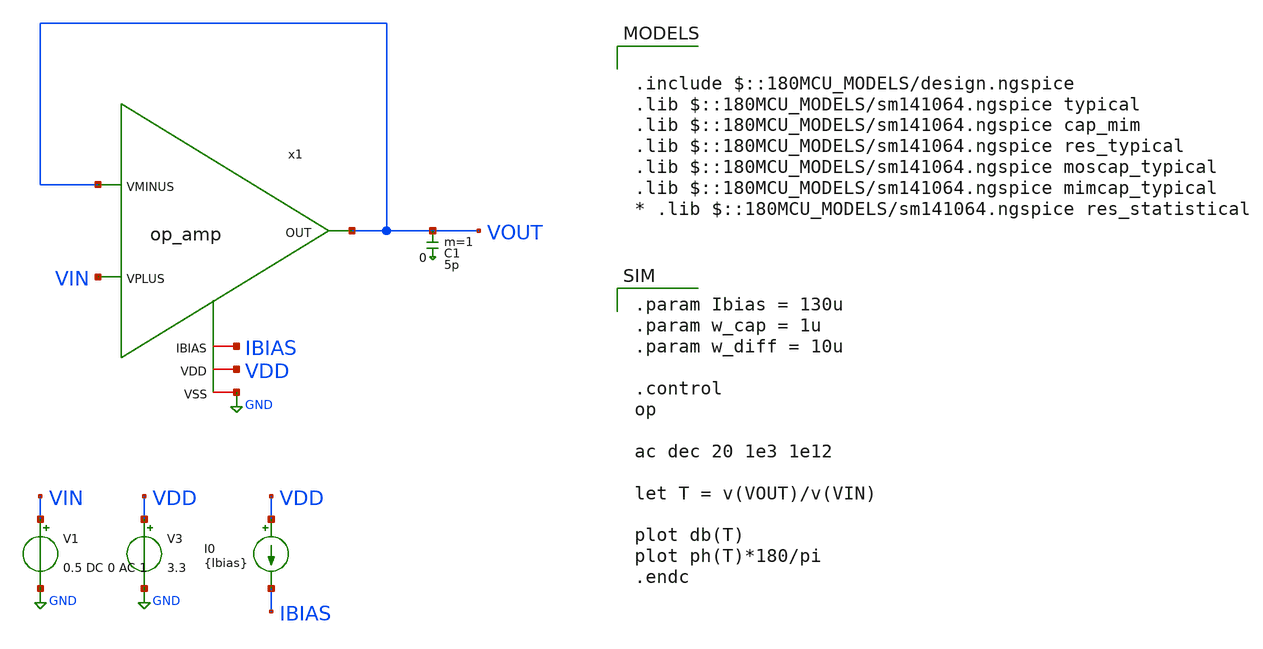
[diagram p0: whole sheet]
** sch_path: xschem/tb_op_amp.sch
**.subckt tb_op_amp
x1 VOUT VIN VOUT VDD GND IBIAS op_amp
V3 VDD GND 3.3
I0 VDD IBIAS {Ibias}
V1 VIN GND 0.5 DC 0 AC 1
C1 VOUT 0 5p m=1
**** begin user architecture code

.param Ibias = 130u
.param w_cap = 1u
.param w_diff = 10u

.control
op

ac dec 20 1e3 1e12

let T = v(VOUT)/v(VIN)

plot db(T)
plot ph(T)*180/pi
.endc



.include $::180MCU_MODELS/design.ngspice
.lib $::180MCU_MODELS/sm141064.ngspice typical
.lib $::180MCU_MODELS/sm141064.ngspice cap_mim
.lib $::180MCU_MODELS/sm141064.ngspice res_typical
.lib $::180MCU_MODELS/sm141064.ngspice moscap_typical
.lib $::180MCU_MODELS/sm141064.ngspice mimcap_typical
* .lib $::180MCU_MODELS/sm141064.ngspice res_statistical

**** end user architecture code
**.ends

* expanding   symbol:  op_amp.sym # of pins=6
** sym_path: xschem/op_amp.sym
** sch_path: xschem/op_amp.sch
.subckt op_amp OUT VPLUS VMINUS VDD VSS IBIAS
*.iopin VDD
*.iopin VSS
*.ipin VPLUS
*.ipin VMINUS
*.opin OUT
*.iopin IBIAS
XM1 net2 VMINUS net1 VSS nfet_03v3 L=0.5u W=4u nf=1 ad='int((nf+1)/2) * W/nf * 0.18u' as='int((nf+2)/2) * W/nf * 0.18u'
+ pd='2*int((nf+1)/2) * (W/nf + 0.18u)' ps='2*int((nf+2)/2) * (W/nf + 0.18u)' nrd='0.18u / W' nrs='0.18u / W'
+ sa=0 sb=0 sd=0 m=1
XM2 net3 VPLUS net1 VSS nfet_03v3 L=0.5u W=4u nf=1 ad='int((nf+1)/2) * W/nf * 0.18u' as='int((nf+2)/2) * W/nf * 0.18u'
+ pd='2*int((nf+1)/2) * (W/nf + 0.18u)' ps='2*int((nf+2)/2) * (W/nf + 0.18u)' nrd='0.18u / W' nrs='0.18u / W'
+ sa=0 sb=0 sd=0 m=1
XM3 net2 net2 VDD VDD pfet_03v3 L=0.5u W=8.5u nf=2 ad='int((nf+1)/2) * W/nf * 0.18u' as='int((nf+2)/2) * W/nf * 0.18u'
+ pd='2*int((nf+1)/2) * (W/nf + 0.18u)' ps='2*int((nf+2)/2) * (W/nf + 0.18u)' nrd='0.18u / W' nrs='0.18u / W'
+ sa=0 sb=0 sd=0 m=1
XM4 net3 net2 VDD VDD pfet_03v3 L=0.5u W=8.5u nf=2 ad='int((nf+1)/2) * W/nf * 0.18u' as='int((nf+2)/2) * W/nf * 0.18u'
+ pd='2*int((nf+1)/2) * (W/nf + 0.18u)' ps='2*int((nf+2)/2) * (W/nf + 0.18u)' nrd='0.18u / W' nrs='0.18u / W'
+ sa=0 sb=0 sd=0 m=1
XM6 net1 IBIAS VSS VSS nfet_03v3 L=0.5u W=6u nf=1 ad='int((nf+1)/2) * W/nf * 0.18u' as='int((nf+2)/2) * W/nf * 0.18u'
+ pd='2*int((nf+1)/2) * (W/nf + 0.18u)' ps='2*int((nf+2)/2) * (W/nf + 0.18u)' nrd='0.18u / W' nrs='0.18u / W'
+ sa=0 sb=0 sd=0 m=1
XM7 OUT net3 VDD VDD pfet_03v3 L=0.5u W=10u nf=20 ad='int((nf+1)/2) * W/nf * 0.18u' as='int((nf+2)/2) * W/nf * 0.18u'
+ pd='2*int((nf+1)/2) * (W/nf + 0.18u)' ps='2*int((nf+2)/2) * (W/nf + 0.18u)' nrd='0.18u / W' nrs='0.18u / W'
+ sa=0 sb=0 sd=0 m=1
XM8 IBIAS IBIAS VSS VSS nfet_03v3 L=0.5u W=6u nf=1 ad='int((nf+1)/2) * W/nf * 0.18u' as='int((nf+2)/2) * W/nf * 0.18u'
+ pd='2*int((nf+1)/2) * (W/nf + 0.18u)' ps='2*int((nf+2)/2) * (W/nf + 0.18u)' nrd='0.18u / W' nrs='0.18u / W'
+ sa=0 sb=0 sd=0 m=1
XM5 OUT IBIAS VSS net4 nfet_03v3 L=0.5u W=7.5u nf=4 ad='int((nf+1)/2) * W/nf * 0.18u' as='int((nf+2)/2) * W/nf * 0.18u'
+ pd='2*int((nf+1)/2) * (W/nf + 0.18u)' ps='2*int((nf+2)/2) * (W/nf + 0.18u)' nrd='0.18u / W' nrs='0.18u / W'
+ sa=0 sb=0 sd=0 m=1
XC1 OUT net3 cap_mim_1f0fF c_width={w_cap} c_length=1e-6 m=1
.ends

.GLOBAL GND
.end
